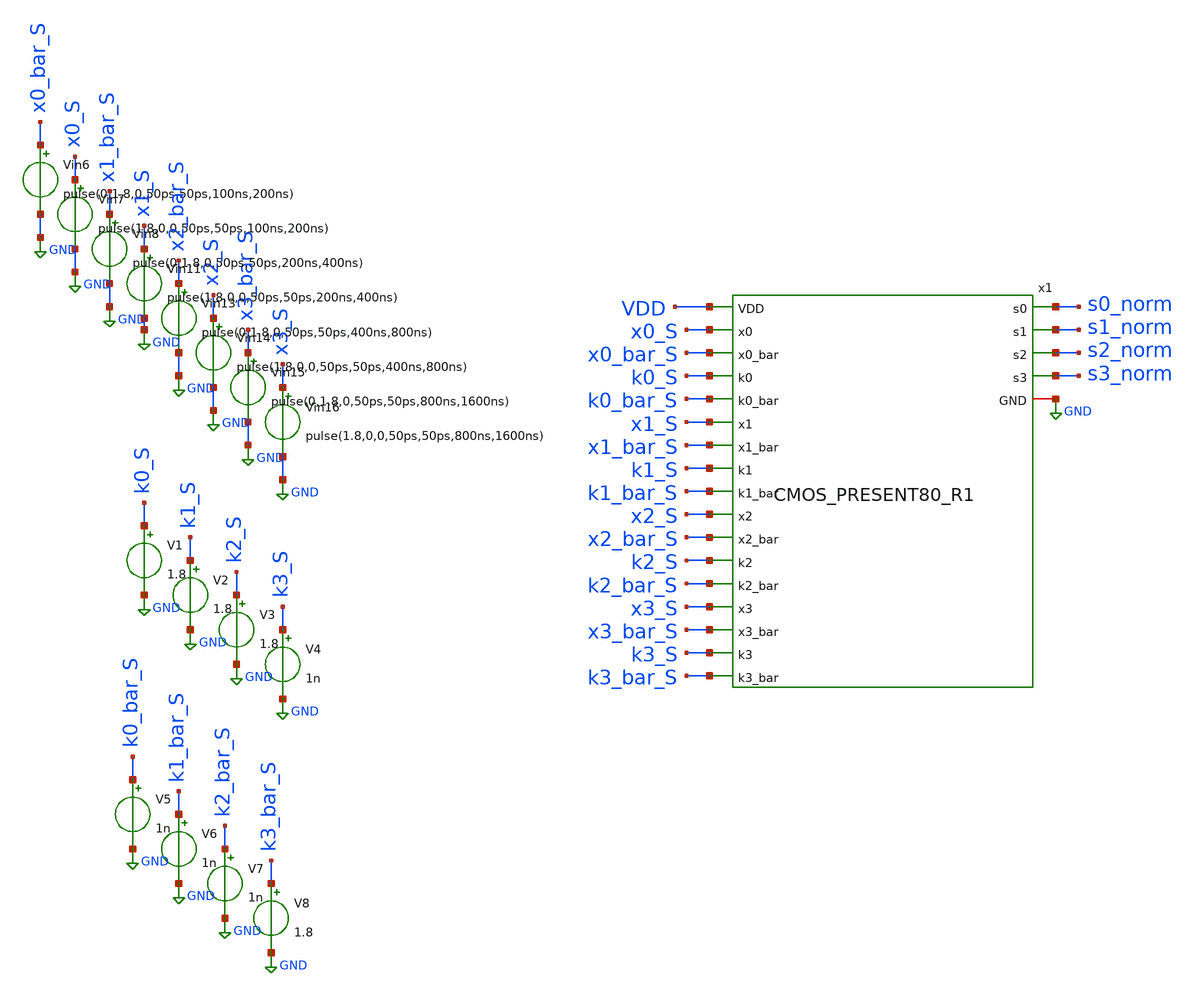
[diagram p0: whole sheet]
** sch_path: skywater_stuff/untitled-18.sch
**.subckt untitled-18
Vin6 x0_bar_S GND pulse(0,1.8,0,50ps,50ps,100ns,200ns)
Vin7 x0_S GND pulse(1.8,0,0,50ps,50ps,100ns,200ns)
Vin8 x1_bar_S GND pulse(0,1.8,0,50ps,50ps,200ns,400ns)
Vin11 x1_S GND pulse(1.8,0,0,50ps,50ps,200ns,400ns)
Vin13 x2_bar_S GND pulse(0,1.8,0,50ps,50ps,400ns,800ns)
Vin14 x2_S GND pulse(1.8,0,0,50ps,50ps,400ns,800ns)
Vin15 x3_bar_S GND pulse(0,1.8,0,50ps,50ps,800ns,1600ns)
Vin16 x3_S GND pulse(1.8,0,0,50ps,50ps,800ns,1600ns)
V1 k0_S GND 1.8
V2 k1_S GND 1.8
V3 k2_S GND 1.8
V4 k3_S GND 1n
V5 k0_bar_S GND 1n
V6 k1_bar_S GND 1n
V7 k2_bar_S GND 1n
V8 k3_bar_S GND 1.8
x1 VDD GND k0_S k0_bar_S x0_S x0_bar_S x1_bar_S x1_S k1_bar_S k1_S k2_S k2_bar_S x2_S x2_bar_S
+ x3_bar_S x3_S k3_bar_S k3_S s3_norm s2_norm s1_norm s0_norm CMOS_PRESENT80_R1
**** begin user architecture code

.lib /research/pdk/open_pdks/share/pdk/sky130A/libs.tech/ngspice/sky130.lib.spice tt
**.include ~/magic_layout_stuff/CMOS_PRESENT80_R1.spice
**.include ~/magic_layout_stuff/CMOS_PRESENT80_R1_flat.spice
.control
save all
tran .1n 10u
**plot v(s0_norm) v(s1_norm) v(s2_norm) v(s3_norm)
**plot v(s0_flat) v(s1_flat) v(s2_flat) v(s3_flat)
plot v(s0_norm)
plot v(s1_norm)
plot v(s2_norm)
plot v(s3_norm)
**plot v(s0_flat)
**plot v(s1_flat)
**plot v(s2_flat)
**plot v(s3_flat)
**plot v(CLK0_S) v(CLK1_S) v(CLK2_S) v(CLK3_S)
plot v(XOR0_S) v(XOR1_S) v(XOR2_S) v(XOR3_S)
plot v(k0_S) v(k1_S) v(k2_S) v(k3_S)
**plot v(XOR0_S)
**plot v(XOR0_bar_S)
**plot v(XOR1_S)
**plot v(XOR1_bar_S)
**plot v(XOR2_S)
**plot v(XOR2_bar_S)
**plot v(XOR3_S)
**plot v(XOR3_bar_S)
**plot v(s0_flat)
**plot v(s1_flat)
**plot v(s2_flat)
**plot v(s3_flat)
**plot v(s0_bar_norm) v(s1_bar_norm) v(s2_bar_norm) v(s3_bar_norm)
**plot v(s0_bar_flat) v(s1_bar_flat) v(s2_bar_flat) v(s3_bar_flat)
**plot v(s0_bar_flat) v(s1_bar_flat) v(s2_bar_flat) v(s3_bar_flat)
**let Pinst_CLK0_CLK3 =
*+ (v(CLK0_S)*i(vclk18))+(v(CLK1_S)*i(vclk22))+(v(CLK2_S)*i(vclk23))+(v(CLK3_S)*i(vclk24))
**let Pinst_CLK0_CLK2_Dis0_Dis2 =
*+ (v(CLK0)*i(vclk0))+(v(Dis0)*i(Vdis0))+(v(CLK1)*i(vclk1))+(v(Dis1)*i(Vdis1))+(v(CLK2)*i(vclk2))+(v(Dis2)*i(Vdis2))
**plot Pinst_CLK0
**plot Pinst_CLK0_CLK3
**wrdata EESPFAL_PRESENT80R1_CLKs.raw v(CLK0_S) v(CLK1_S) v(CLK2_S) v(CLK3_S)
wrdata EESPFAL_PRESENT80R1_X_inputs.raw v(XOR0_S) v(XOR1_S) v(XOR2_S) v(XOR3_S)
wrdata EESPFAL_PRESENT80R1_K_inputs.raw v(k0_S) v(k1_S) v(k2_S) v(k3_S)
wrdata EESPFAL_PRESENT80R1_InstPWR.raw Pinst_CLK0_CLK3
**wrdata EESPFAL_PRESENT80_R1.raw v(s0_norm) v(s1_norm) v(s2_norm) v(s3_norm) v(s0_bar_norm)
*+ v(s1_bar_norm) v(s2_bar_norm) v(s3_bar_norm)
**wrdata EESPFAL_PRESENT80_R1_PEX.raw v(s0_flat) v(s1_flat) v(s2_flat) v(s3_flat) v(s0_bar_flat)
*+ v(s1_bar_flat) v(s2_bar_flat) v(s3_bar_flat)
**wrdata EESPFAL_PRESENT80_R1.csv v(s0_norm) v(s1_norm) v(s2_norm) v(s3_norm) v(s0_bar_norm)
*+ v(s1_bar_norm) v(s2_bar_norm) v(s3_bar_norm)
*wrdata EESPFAL_PRESENT80_R1_PEX.csv v(s0_flat) v(s1_flat) v(s2_flat) v(s3_flat) v(s0_bar_flat)
*+ v(s1_bar_flat) v(s2_bar_flat) v(s3_bar_flat)
**wrdata EESPFAL_PRESENT80_R1_PEX_PWR.raw Pinst_CLK0_CLK3
**wrdata EESPFAL_PRESENT80_R1_PEX_PWR.csv Pinst_CLK0_CLK3
**wrdata EESPFAL_PRESENT80_R1.raw
.endc


**** end user architecture code
**.ends
.GLOBAL GND
.end
